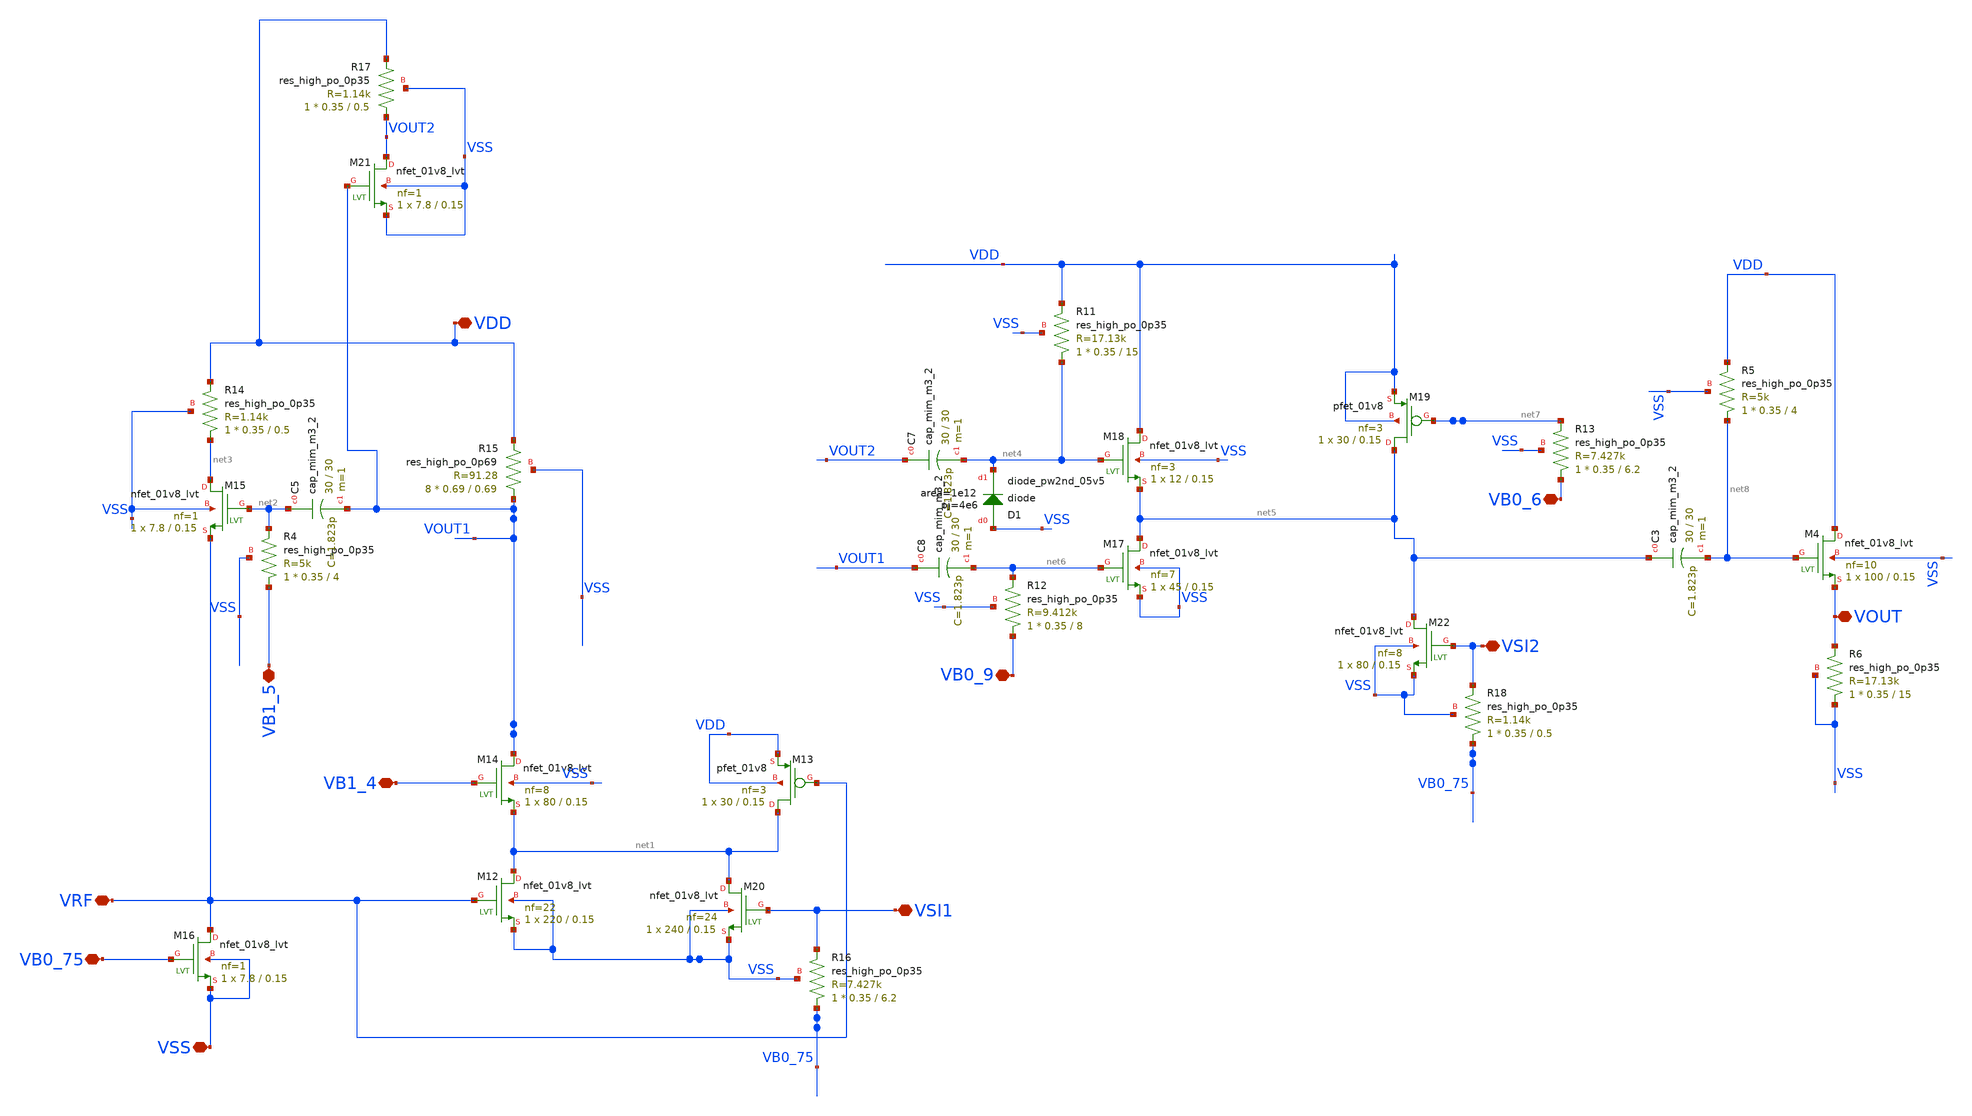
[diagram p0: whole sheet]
** sch_path: xschem/xschem4_sic_oct_20/partitions5_individual_for_Symbol.sch
**.subckt partitions5_individual_for_Symbol VRF VSS VB0_75 VSI1 VB1_4 VDD VB1_5 VB0_9 VSI2 VB0_6
*+ VOUT
*.iopin VRF
*.iopin VSS
*.iopin VB0_75
*.iopin VSI1
*.iopin VB1_4
*.iopin VDD
*.iopin VB1_5
*.iopin VB0_9
*.iopin VSI2
*.iopin VB0_6
*.iopin VOUT
XM12 net1 VRF VSS VSS sky130_fd_pr__nfet_01v8_lvt L=0.15 W=220 nf=22 ad='int((nf+1)/2) * W/nf * 0.29'
+ as='int((nf+2)/2) * W/nf * 0.29' pd='2*int((nf+1)/2) * (W/nf + 0.29)' ps='2*int((nf+2)/2) * (W/nf + 0.29)'
+ nrd='0.29 / W' nrs='0.29 / W' sa=0 sb=0 sd=0 mult=1 m=1
XM13 net1 VRF VDD VDD sky130_fd_pr__pfet_01v8 L=0.15 W=30 nf=3 ad='int((nf+1)/2) * W/nf * 0.29' as='int((nf+2)/2) * W/nf * 0.29'
+ pd='2*int((nf+1)/2) * (W/nf + 0.29)' ps='2*int((nf+2)/2) * (W/nf + 0.29)' nrd='0.29 / W' nrs='0.29 / W'
+ sa=0 sb=0 sd=0 mult=1 m=1
XM14 VOUT1 VB1_4 net1 VSS sky130_fd_pr__nfet_01v8_lvt L=0.15 W=80 nf=8 ad='int((nf+1)/2) * W/nf * 0.29'
+ as='int((nf+2)/2) * W/nf * 0.29' pd='2*int((nf+1)/2) * (W/nf + 0.29)' ps='2*int((nf+2)/2) * (W/nf + 0.29)'
+ nrd='0.29 / W' nrs='0.29 / W' sa=0 sb=0 sd=0 mult=1 m=1
XM16 VRF VB0_75 VSS VSS sky130_fd_pr__nfet_01v8_lvt L=0.15 W=7.8 nf=1 ad='int((nf+1)/2) * W/nf * 0.29'
+ as='int((nf+2)/2) * W/nf * 0.29' pd='2*int((nf+1)/2) * (W/nf + 0.29)' ps='2*int((nf+2)/2) * (W/nf + 0.29)'
+ nrd='0.29 / W' nrs='0.29 / W' sa=0 sb=0 sd=0 mult=1 m=1
XM20 net1 VSI1 VSS VSS sky130_fd_pr__nfet_01v8_lvt L=0.15 W=240 nf=24 ad='int((nf+1)/2) * W/nf * 0.29'
+ as='int((nf+2)/2) * W/nf * 0.29' pd='2*int((nf+1)/2) * (W/nf + 0.29)' ps='2*int((nf+2)/2) * (W/nf + 0.29)'
+ nrd='0.29 / W' nrs='0.29 / W' sa=0 sb=0 sd=0 mult=1 m=1
XR16 VB0_75 VSI1 VSS sky130_fd_pr__res_high_po_0p35 L=6.2 mult=1 m=1
XR4 VB1_5 net2 VSS sky130_fd_pr__res_high_po_0p35 L=4 mult=1 m=1
XC5 net2 VOUT1 sky130_fd_pr__cap_mim_m3_2 W=30 L=30 MF=1 m=1
XM15 net3 net2 VRF VSS sky130_fd_pr__nfet_01v8_lvt L=0.15 W=7.8 nf=1 ad='int((nf+1)/2) * W/nf * 0.29'
+ as='int((nf+2)/2) * W/nf * 0.29' pd='2*int((nf+1)/2) * (W/nf + 0.29)' ps='2*int((nf+2)/2) * (W/nf + 0.29)'
+ nrd='0.29 / W' nrs='0.29 / W' sa=0 sb=0 sd=0 mult=1 m=1
XR14 net3 VDD VSS sky130_fd_pr__res_high_po_0p35 L=0.5 mult=1 m=1
XR15 VOUT1 VDD VSS sky130_fd_pr__res_high_po_0p69 L=0.69 mult=8 m=8
XM21 VOUT2 VOUT1 VSS VSS sky130_fd_pr__nfet_01v8_lvt L=0.15 W=7.8 nf=1 ad='int((nf+1)/2) * W/nf * 0.29'
+ as='int((nf+2)/2) * W/nf * 0.29' pd='2*int((nf+1)/2) * (W/nf + 0.29)' ps='2*int((nf+2)/2) * (W/nf + 0.29)'
+ nrd='0.29 / W' nrs='0.29 / W' sa=0 sb=0 sd=0 mult=1 m=1
XR17 VOUT2 VDD VSS sky130_fd_pr__res_high_po_0p35 L=0.5 mult=1 m=1
XM17 net5 net6 VSS VSS sky130_fd_pr__nfet_01v8_lvt L=0.15 W=45 nf=7 ad='int((nf+1)/2) * W/nf * 0.29'
+ as='int((nf+2)/2) * W/nf * 0.29' pd='2*int((nf+1)/2) * (W/nf + 0.29)' ps='2*int((nf+2)/2) * (W/nf + 0.29)'
+ nrd='0.29 / W' nrs='0.29 / W' sa=0 sb=0 sd=0 mult=1 m=1
XM18 VDD net4 net5 VSS sky130_fd_pr__nfet_01v8_lvt L=0.15 W=12 nf=3 ad='int((nf+1)/2) * W/nf * 0.29'
+ as='int((nf+2)/2) * W/nf * 0.29' pd='2*int((nf+1)/2) * (W/nf + 0.29)' ps='2*int((nf+2)/2) * (W/nf + 0.29)'
+ nrd='0.29 / W' nrs='0.29 / W' sa=0 sb=0 sd=0 mult=1 m=1
XR11 net4 VDD VSS sky130_fd_pr__res_high_po_0p35 L=15 mult=1 m=1
XC7 VOUT2 net4 sky130_fd_pr__cap_mim_m3_2 W=30 L=30 MF=1 m=1
XR12 VB0_9 net6 VSS sky130_fd_pr__res_high_po_0p35 L=8 mult=1 m=1
XC8 VOUT1 net6 sky130_fd_pr__cap_mim_m3_2 W=30 L=30 MF=1 m=1
XD1 VSS net4 sky130_fd_pr__diode_pw2nd_05v5 area=1e12 pj=4e6
XM19 net5 net7 VDD VDD sky130_fd_pr__pfet_01v8 L=0.15 W=30 nf=3 ad='int((nf+1)/2) * W/nf * 0.29' as='int((nf+2)/2) * W/nf * 0.29'
+ pd='2*int((nf+1)/2) * (W/nf + 0.29)' ps='2*int((nf+2)/2) * (W/nf + 0.29)' nrd='0.29 / W' nrs='0.29 / W'
+ sa=0 sb=0 sd=0 mult=1 m=1
XR13 VB0_6 net7 VSS sky130_fd_pr__res_high_po_0p35 L=6.2 mult=1 m=1
XM22 net5 VSI2 VSS VSS sky130_fd_pr__nfet_01v8_lvt L=0.15 W=80 nf=8 ad='int((nf+1)/2) * W/nf * 0.29'
+ as='int((nf+2)/2) * W/nf * 0.29' pd='2*int((nf+1)/2) * (W/nf + 0.29)' ps='2*int((nf+2)/2) * (W/nf + 0.29)'
+ nrd='0.29 / W' nrs='0.29 / W' sa=0 sb=0 sd=0 mult=1 m=1
XR18 VB0_75 VSI2 VSS sky130_fd_pr__res_high_po_0p35 L=0.5 mult=1 m=1
XM4 VDD net8 VOUT VSS sky130_fd_pr__nfet_01v8_lvt L=0.15 W=100 nf=10 ad='int((nf+1)/2) * W/nf * 0.29'
+ as='int((nf+2)/2) * W/nf * 0.29' pd='2*int((nf+1)/2) * (W/nf + 0.29)' ps='2*int((nf+2)/2) * (W/nf + 0.29)'
+ nrd='0.29 / W' nrs='0.29 / W' sa=0 sb=0 sd=0 mult=1 m=1
XR5 net8 VDD VSS sky130_fd_pr__res_high_po_0p35 L=4 mult=1 m=1
XR6 VSS VOUT VSS sky130_fd_pr__res_high_po_0p35 L=15 mult=1 m=1
XC3 net5 net8 sky130_fd_pr__cap_mim_m3_2 W=30 L=30 MF=1 m=1
**.ends
.end
